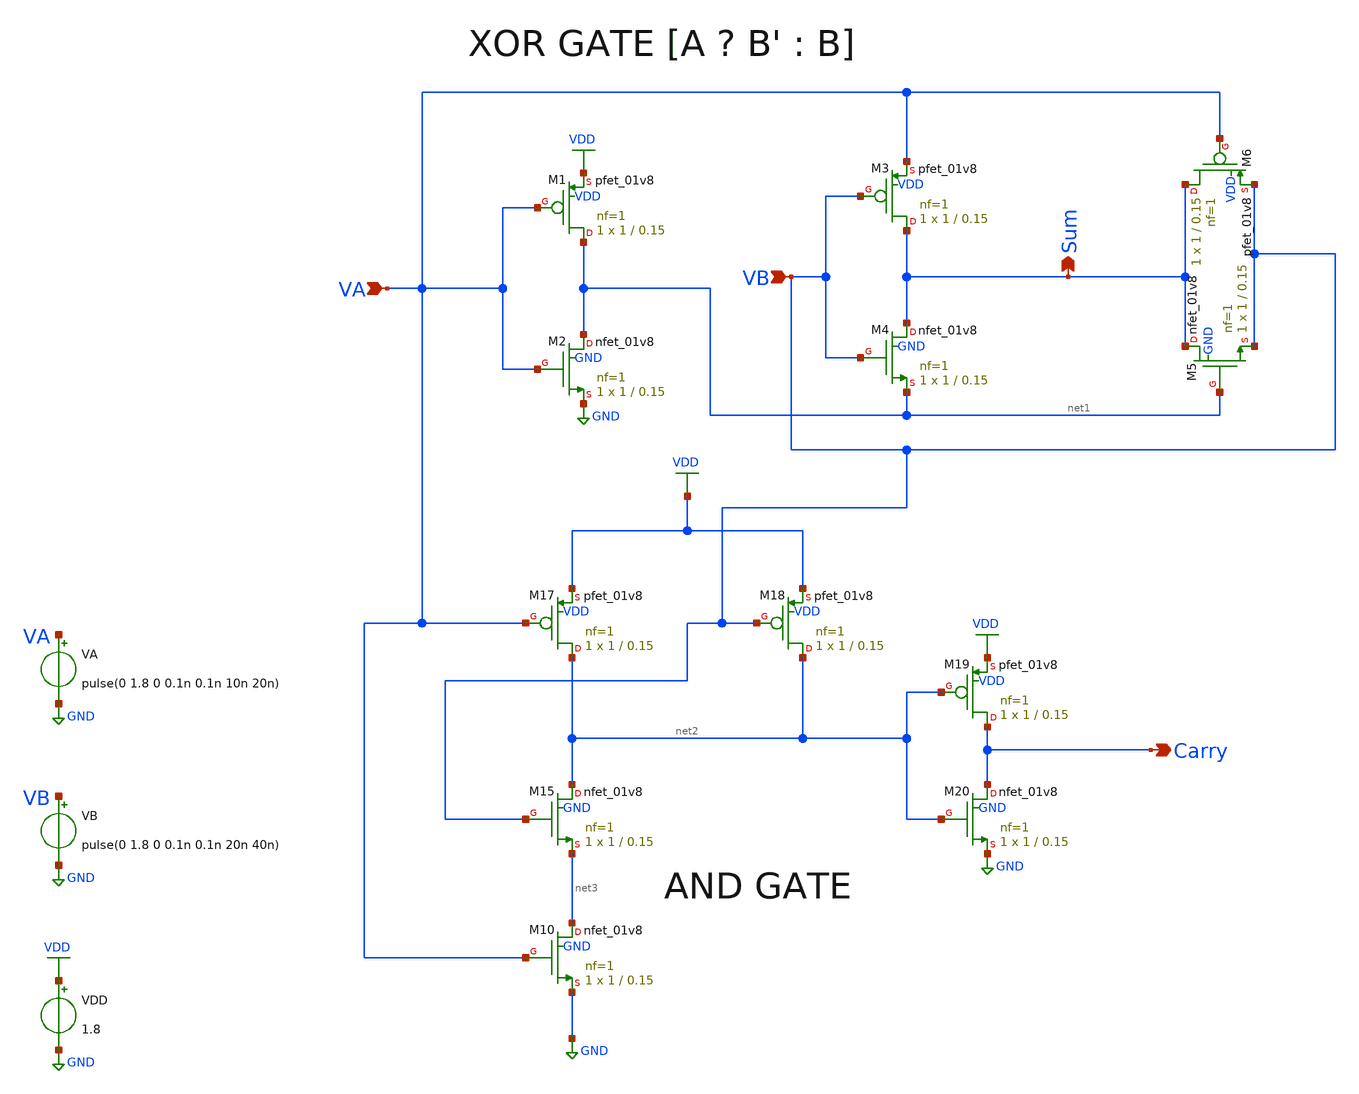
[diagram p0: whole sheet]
** sch_path: units/top/ana/blocks/half_adder/half_adder_TG.sch
**.subckt half_adder_TG VA VB Sum Carry
*.ipin VA
*.ipin VB
*.opin Sum
*.opin Carry
XM1 net1 VA VDD VDD sky130_fd_pr__pfet_01v8 L=0.15 W=1 nf=1 ad='int((1 + 1)/2) * 1 / 1 * 0.29' as='int((1 + 2)/2) * 1 / 1 * 0.29'
+ pd='2*int((1 + 1)/2) * (1 / 1 + 0.29)' ps='2*int((1 + 2)/2) * (1 / 1 + 0.29)' nrd='0.29 / 1 ' nrs='0.29 / 1 '
+ sa=0 sb=0 sd=0 mult=1 m=1
XM2 net1 VA GND GND sky130_fd_pr__nfet_01v8 L=0.15 W=1 nf=1 ad='int((1 + 1)/2) * 1 / 1 * 0.29' as='int((1 + 2)/2) * 1 / 1 * 0.29'
+ pd='2*int((1 + 1)/2) * (1 / 1 + 0.29)' ps='2*int((1 + 2)/2) * (1 / 1 + 0.29)' nrd='0.29 / 1 ' nrs='0.29 / 1 '
+ sa=0 sb=0 sd=0 mult=1 m=1
VB VB GND pulse(0 1.8 0 0.1n 0.1n 20n 40n)
VA VA GND pulse(0 1.8 0 0.1n 0.1n 10n 20n)
XM3 Sum VB VA VDD sky130_fd_pr__pfet_01v8 L=0.15 W=1 nf=1 ad='int((1 + 1)/2) * 1 / 1 * 0.29' as='int((1 + 2)/2) * 1 / 1 * 0.29'
+ pd='2*int((1 + 1)/2) * (1 / 1 + 0.29)' ps='2*int((1 + 2)/2) * (1 / 1 + 0.29)' nrd='0.29 / 1 ' nrs='0.29 / 1 '
+ sa=0 sb=0 sd=0 mult=1 m=1
XM4 Sum VB net1 GND sky130_fd_pr__nfet_01v8 L=0.15 W=1 nf=1 ad='int((1 + 1)/2) * 1 / 1 * 0.29' as='int((1 + 2)/2) * 1 / 1 * 0.29'
+ pd='2*int((1 + 1)/2) * (1 / 1 + 0.29)' ps='2*int((1 + 2)/2) * (1 / 1 + 0.29)' nrd='0.29 / 1 ' nrs='0.29 / 1 '
+ sa=0 sb=0 sd=0 mult=1 m=1
XM5 Sum net1 VB GND sky130_fd_pr__nfet_01v8 L=0.15 W=1 nf=1 ad='int((1 + 1)/2) * 1 / 1 * 0.29' as='int((1 + 2)/2) * 1 / 1 * 0.29'
+ pd='2*int((1 + 1)/2) * (1 / 1 + 0.29)' ps='2*int((1 + 2)/2) * (1 / 1 + 0.29)' nrd='0.29 / 1 ' nrs='0.29 / 1 '
+ sa=0 sb=0 sd=0 mult=1 m=1
XM6 Sum VA VB VDD sky130_fd_pr__pfet_01v8 L=0.15 W=1 nf=1 ad='int((1 + 1)/2) * 1 / 1 * 0.29' as='int((1 + 2)/2) * 1 / 1 * 0.29'
+ pd='2*int((1 + 1)/2) * (1 / 1 + 0.29)' ps='2*int((1 + 2)/2) * (1 / 1 + 0.29)' nrd='0.29 / 1 ' nrs='0.29 / 1 '
+ sa=0 sb=0 sd=0 mult=1 m=1
XM10 net3 VA GND GND sky130_fd_pr__nfet_01v8 L=0.15 W=1 nf=1 ad='int((1 + 1)/2) * 1 / 1 * 0.29' as='int((1 + 2)/2) * 1 / 1 * 0.29'
+ pd='2*int((1 + 1)/2) * (1 / 1 + 0.29)' ps='2*int((1 + 2)/2) * (1 / 1 + 0.29)' nrd='0.29 / 1 ' nrs='0.29 / 1 '
+ sa=0 sb=0 sd=0 mult=1 m=1
XM15 net2 VB net3 GND sky130_fd_pr__nfet_01v8 L=0.15 W=1 nf=1 ad='int((1 + 1)/2) * 1 / 1 * 0.29' as='int((1 + 2)/2) * 1 / 1 * 0.29'
+ pd='2*int((1 + 1)/2) * (1 / 1 + 0.29)' ps='2*int((1 + 2)/2) * (1 / 1 + 0.29)' nrd='0.29 / 1 ' nrs='0.29 / 1 '
+ sa=0 sb=0 sd=0 mult=1 m=1
XM17 net2 VA VDD VDD sky130_fd_pr__pfet_01v8 L=0.15 W=1 nf=1 ad='int((1 + 1)/2) * 1 / 1 * 0.29' as='int((1 + 2)/2) * 1 / 1 * 0.29'
+ pd='2*int((1 + 1)/2) * (1 / 1 + 0.29)' ps='2*int((1 + 2)/2) * (1 / 1 + 0.29)' nrd='0.29 / 1 ' nrs='0.29 / 1 '
+ sa=0 sb=0 sd=0 mult=1 m=1
XM18 net2 VB VDD VDD sky130_fd_pr__pfet_01v8 L=0.15 W=1 nf=1 ad='int((1 + 1)/2) * 1 / 1 * 0.29' as='int((1 + 2)/2) * 1 / 1 * 0.29'
+ pd='2*int((1 + 1)/2) * (1 / 1 + 0.29)' ps='2*int((1 + 2)/2) * (1 / 1 + 0.29)' nrd='0.29 / 1 ' nrs='0.29 / 1 '
+ sa=0 sb=0 sd=0 mult=1 m=1
XM19 Carry net2 VDD VDD sky130_fd_pr__pfet_01v8 L=0.15 W=1 nf=1 ad='int((1 + 1)/2) * 1 / 1 * 0.29' as='int((1 + 2)/2) * 1 / 1 * 0.29'
+ pd='2*int((1 + 1)/2) * (1 / 1 + 0.29)' ps='2*int((1 + 2)/2) * (1 / 1 + 0.29)' nrd='0.29 / 1 ' nrs='0.29 / 1 '
+ sa=0 sb=0 sd=0 mult=1 m=1
XM20 Carry net2 GND GND sky130_fd_pr__nfet_01v8 L=0.15 W=1 nf=1 ad='int((1 + 1)/2) * 1 / 1 * 0.29' as='int((1 + 2)/2) * 1 / 1 * 0.29'
+ pd='2*int((1 + 1)/2) * (1 / 1 + 0.29)' ps='2*int((1 + 2)/2) * (1 / 1 + 0.29)' nrd='0.29 / 1 ' nrs='0.29 / 1 '
+ sa=0 sb=0 sd=0 mult=1 m=1
VDD VDD GND 1.8
.save i(vdd)
**** begin user architecture code

.lib /usr/local/share/pdk/sky130B/libs.tech/ngspice/sky130.lib.spice tt
.option wnflag=1

**** end user architecture code
**.ends
.GLOBAL GND
.GLOBAL VDD
**** begin user architecture code


.save v(VA) v(VB) v(Sum) v(Carry)
.tran 0.1n 200n


**** end user architecture code
.end
